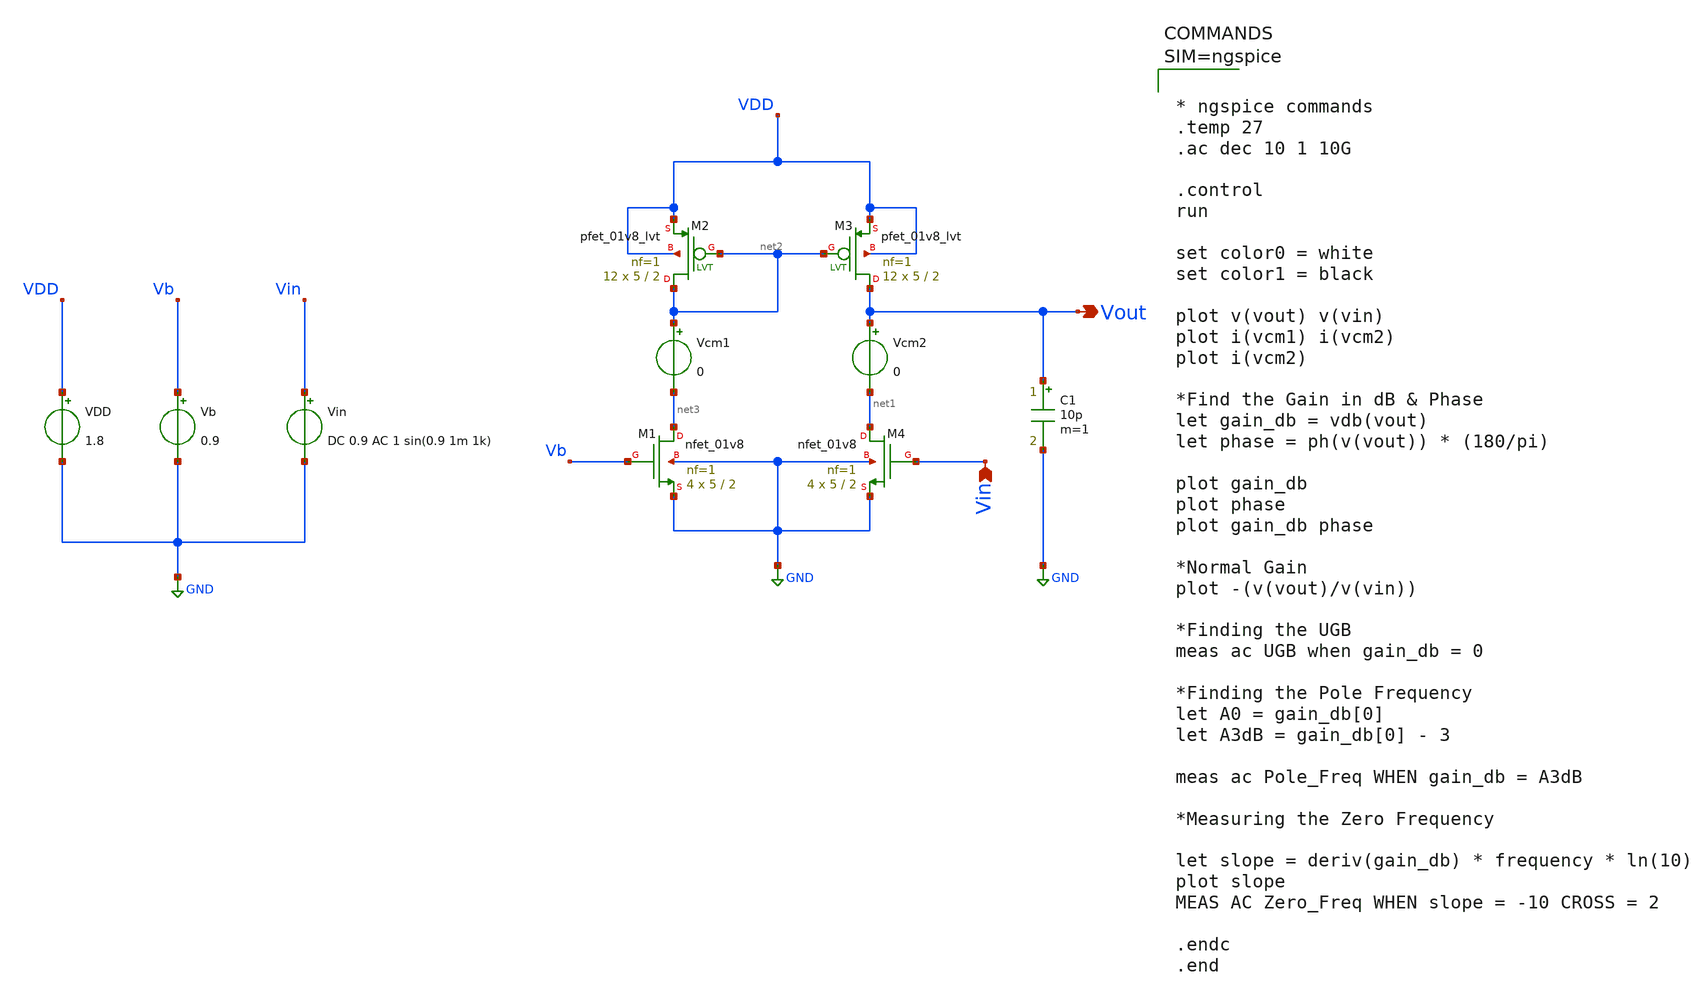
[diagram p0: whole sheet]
** sch_path: Common_Source_PMOS_Current_Source_Load_ckts/CS_Amp_PMOS_Current_Source_Load_AC_Analysis_ckt.sch
**.subckt CS_Amp_PMOS_Current_Source_Load_AC_Analysis_ckt Vout Vin
*.opin Vout
*.ipin Vin
XM1 net3 Vb GND GND sky130_fd_pr__nfet_01v8 L=2 W=5 nf=1 ad='int((1 + 1)/2) * 5 / 1 * 0.29' as='int((1 + 2)/2) * 5 / 1 * 0.29'
+ pd='2*int((1 + 1)/2) * (5 / 1 + 0.29)' ps='2*int((1 + 2)/2) * (5 / 1 + 0.29)' nrd='0.29 / 5 ' nrs='0.29 / 5 '
+ sa=0 sb=0 sd=0 mult=4 m=4
XM2 net2 net2 VDD VDD sky130_fd_pr__pfet_01v8_lvt L=2 W=5 nf=1 ad='int((1 + 1)/2) * 5 / 1 * 0.29' as='int((1 + 2)/2) * 5 / 1 * 0.29'
+ pd='2*int((1 + 1)/2) * (5 / 1 + 0.29)' ps='2*int((1 + 2)/2) * (5 / 1 + 0.29)' nrd='0.29 / 5 ' nrs='0.29 / 5 '
+ sa=0 sb=0 sd=0 mult=12 m=12
XM3 Vout net2 VDD VDD sky130_fd_pr__pfet_01v8_lvt L=2 W=5 nf=1 ad='int((1 + 1)/2) * 5 / 1 * 0.29' as='int((1 + 2)/2) * 5 / 1 * 0.29'
+ pd='2*int((1 + 1)/2) * (5 / 1 + 0.29)' ps='2*int((1 + 2)/2) * (5 / 1 + 0.29)' nrd='0.29 / 5 ' nrs='0.29 / 5 '
+ sa=0 sb=0 sd=0 mult=12 m=12
XM4 net1 Vin GND GND sky130_fd_pr__nfet_01v8 L=2 W=5 nf=1 ad='int((1 + 1)/2) * 5 / 1 * 0.29' as='int((1 + 2)/2) * 5 / 1 * 0.29'
+ pd='2*int((1 + 1)/2) * (5 / 1 + 0.29)' ps='2*int((1 + 2)/2) * (5 / 1 + 0.29)' nrd='0.29 / 5 ' nrs='0.29 / 5 '
+ sa=0 sb=0 sd=0 mult=4 m=4
Vb Vb GND 0.9
Vin Vin GND DC 0.9 AC 1 sin(0.9 1m 1k)
VDD VDD GND 1.8
Vcm1 net2 net3 0
Vcm2 Vout net1 0
C1 Vout GND 10p m=1
**** begin user architecture code



* ngspice commands
.temp 27
.ac dec 10 1 10G

.control
run

set color0 = white
set color1 = black

plot v(vout) v(vin)
plot i(vcm1) i(vcm2)
plot i(vcm2)

*Find the Gain in dB & Phase
let gain_db = vdb(vout)
let phase = ph(v(vout)) * (180/pi)

plot gain_db
plot phase
plot gain_db phase

*Normal Gain
plot -(v(vout)/v(vin))

*Finding the UGB
meas ac UGB when gain_db = 0

*Finding the Pole Frequency
let A0 = gain_db[0]
let A3dB = gain_db[0] - 3

meas ac Pole_Freq WHEN gain_db = A3dB

*Measuring the Zero Frequency

let slope = deriv(gain_db) * frequency * ln(10)
plot slope
MEAS AC Zero_Freq WHEN slope = -10 CROSS = 2

.endc
.end






** opencircuitdesign pdks install
.lib $::SKYWATER_MODELS/sky130.lib.spice tt

**** end user architecture code
**.ends
.GLOBAL GND
.end
